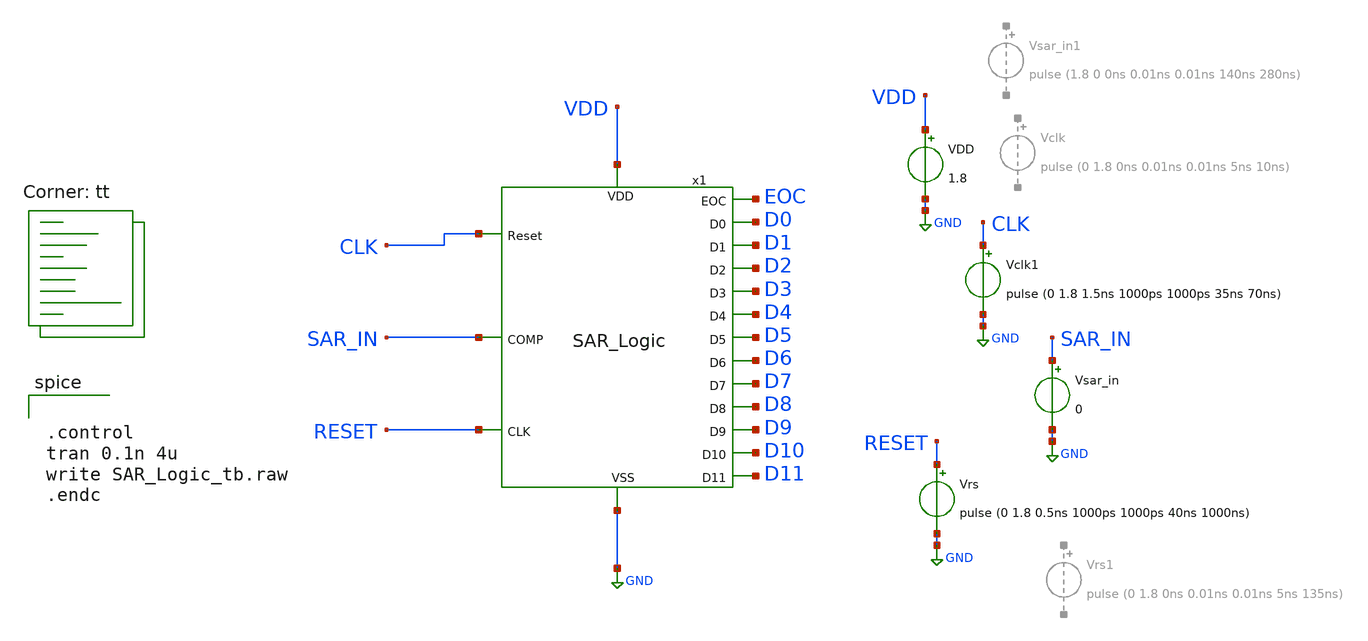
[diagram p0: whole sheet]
** sch_path: SAR_Logic_tb.sch
**.subckt SAR_Logic_tb
x1 EOC RESET SAR_IN VDD GND CLK D9 D4 D10 D5 D6 D3 D2 D1 D0 D7 D8 D11 SAR_Logic
VDD VDD GND 1.8
Vsar_in SAR_IN GND 0
Vrs RESET GND pulse (0 1.8 0.5ns 1000ps 1000ps 40ns 1000ns)
Vclk1 CLK GND pulse (0 1.8 1.5ns 1000ps 1000ps 35ns 70ns)
**** begin user architecture code
.lib $::SKYWATER_MODELS/sky130.lib.spice tt


.control
tran 0.1n 4u
write SAR_Logic_tb.raw
.endc

**** end user architecture code
**.ends
.GLOBAL GND
.end
